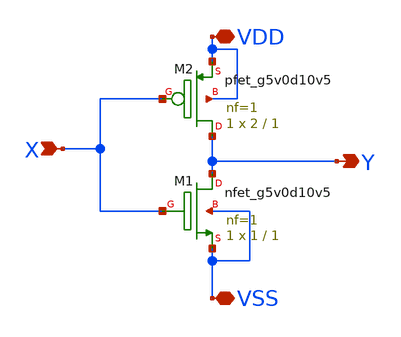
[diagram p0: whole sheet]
** sch_path: ADC/16bit_C2C/MagicAndSpice/NOT5V.sch
**.subckt NOT5V X Y VSS VDD
*.ipin X
*.opin Y
*.iopin VSS
*.iopin VDD
XM1 Y X VSS VSS sky130_fd_pr__nfet_g5v0d10v5 L=1 W=1 nf=1 ad='int((nf+1)/2) * W/nf * 0.29' as='int((nf+2)/2) * W/nf * 0.29'
+ pd='2*int((nf+1)/2) * (W/nf + 0.29)' ps='2*int((nf+2)/2) * (W/nf + 0.29)' nrd='0.29 / W' nrs='0.29 / W'
+ sa=0 sb=0 sd=0 mult=1 m=1
XM2 Y X VDD VDD sky130_fd_pr__pfet_g5v0d10v5 L=1 W=2 nf=1 ad='int((nf+1)/2) * W/nf * 0.29' as='int((nf+2)/2) * W/nf * 0.29'
+ pd='2*int((nf+1)/2) * (W/nf + 0.29)' ps='2*int((nf+2)/2) * (W/nf + 0.29)' nrd='0.29 / W' nrs='0.29 / W'
+ sa=0 sb=0 sd=0 mult=1 m=1
**.ends
.end
